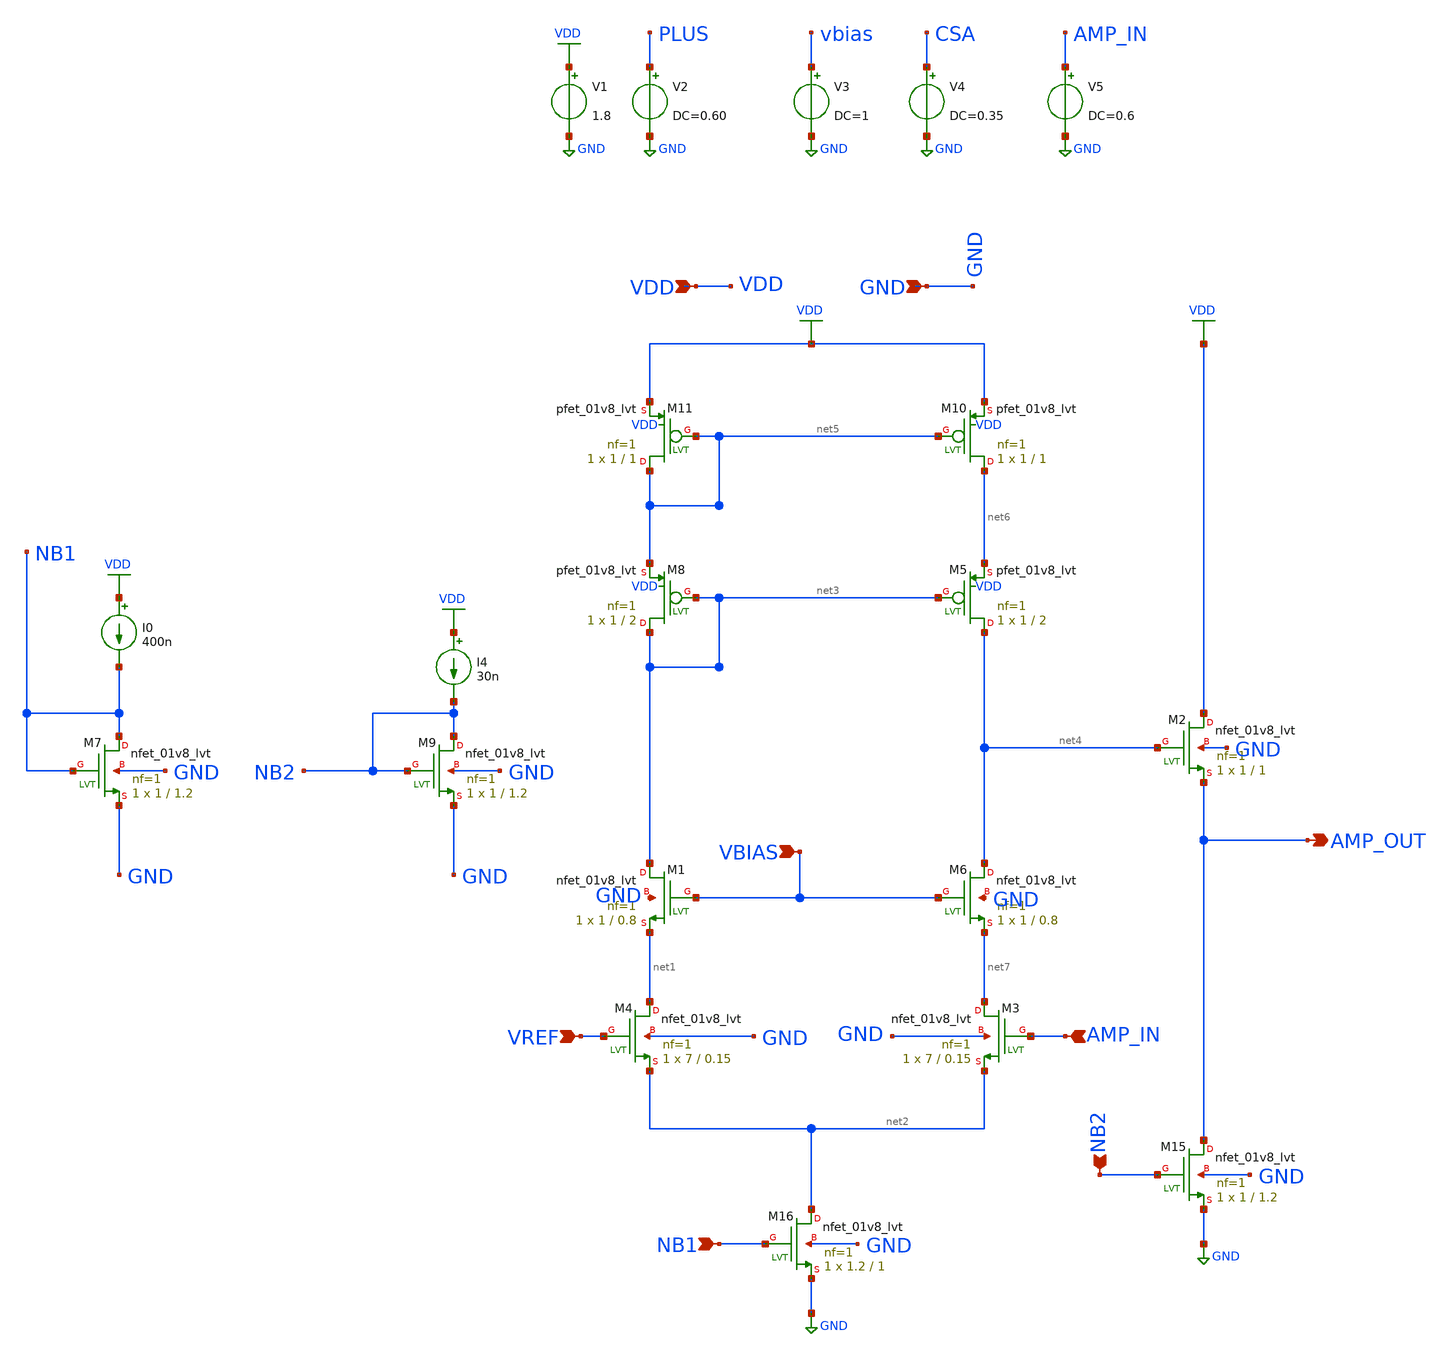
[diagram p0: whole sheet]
** sch_path: xschem/testbench/nmos_cs.sch
**.subckt nmos_cs VREF AMP_IN NB1 VBIAS VDD GND AMP_OUT NB2
*.ipin VREF
*.ipin AMP_IN
*.ipin NB1
*.ipin VBIAS
*.ipin VDD
*.ipin GND
*.opin AMP_OUT
*.ipin NB2
V1 VDD GND 1.8
V2 PLUS GND DC=0.60
V3 vbias GND DC=1
V4 CSA GND DC=0.35
XM8 net3 net3 net5 VDD sky130_fd_pr__pfet_01v8_lvt L=2 W=1 nf=1 ad='int((nf+1)/2) * W/nf * 0.29' as='int((nf+2)/2) * W/nf * 0.29'
+ pd='2*int((nf+1)/2) * (W/nf + 0.29)' ps='2*int((nf+2)/2) * (W/nf + 0.29)' nrd='0.29 / W' nrs='0.29 / W'
+ sa=0 sb=0 sd=0 mult=1 m=1
XM10 net6 net5 VDD VDD sky130_fd_pr__pfet_01v8_lvt L=1 W=1 nf=1 ad='int((nf+1)/2) * W/nf * 0.29' as='int((nf+2)/2) * W/nf * 0.29'
+ pd='2*int((nf+1)/2) * (W/nf + 0.29)' ps='2*int((nf+2)/2) * (W/nf + 0.29)' nrd='0.29 / W' nrs='0.29 / W'
+ sa=0 sb=0 sd=0 mult=1 m=1
XM11 net5 net5 VDD VDD sky130_fd_pr__pfet_01v8_lvt L=1 W=1 nf=1 ad='int((nf+1)/2) * W/nf * 0.29' as='int((nf+2)/2) * W/nf * 0.29'
+ pd='2*int((nf+1)/2) * (W/nf + 0.29)' ps='2*int((nf+2)/2) * (W/nf + 0.29)' nrd='0.29 / W' nrs='0.29 / W'
+ sa=0 sb=0 sd=0 mult=1 m=1
XM16 net2 NB1 GND GND sky130_fd_pr__nfet_01v8_lvt L=1 W=1.2 nf=1 ad='int((nf+1)/2) * W/nf * 0.29' as='int((nf+2)/2) * W/nf * 0.29'
+ pd='2*int((nf+1)/2) * (W/nf + 0.29)' ps='2*int((nf+2)/2) * (W/nf + 0.29)' nrd='0.29 / W' nrs='0.29 / W'
+ sa=0 sb=0 sd=0 mult=1 m=1
XM4 net1 VREF net2 GND sky130_fd_pr__nfet_01v8_lvt L=0.15 W=7 nf=1 ad='int((nf+1)/2) * W/nf * 0.29' as='int((nf+2)/2) * W/nf * 0.29'
+ pd='2*int((nf+1)/2) * (W/nf + 0.29)' ps='2*int((nf+2)/2) * (W/nf + 0.29)' nrd='0.29 / W' nrs='0.29 / W'
+ sa=0 sb=0 sd=0 mult=1 m=1
XM5 net4 net3 net6 VDD sky130_fd_pr__pfet_01v8_lvt L=2 W=1 nf=1 ad='int((nf+1)/2) * W/nf * 0.29' as='int((nf+2)/2) * W/nf * 0.29'
+ pd='2*int((nf+1)/2) * (W/nf + 0.29)' ps='2*int((nf+2)/2) * (W/nf + 0.29)' nrd='0.29 / W' nrs='0.29 / W'
+ sa=0 sb=0 sd=0 mult=1 m=1
XM1 net3 VBIAS net1 GND sky130_fd_pr__nfet_01v8_lvt L=0.8 W=1 nf=1 ad='int((nf+1)/2) * W/nf * 0.29' as='int((nf+2)/2) * W/nf * 0.29'
+ pd='2*int((nf+1)/2) * (W/nf + 0.29)' ps='2*int((nf+2)/2) * (W/nf + 0.29)' nrd='0.29 / W' nrs='0.29 / W'
+ sa=0 sb=0 sd=0 mult=1 m=1
XM3 net7 AMP_IN net2 GND sky130_fd_pr__nfet_01v8_lvt L=0.15 W=7 nf=1 ad='int((nf+1)/2) * W/nf * 0.29'
+ as='int((nf+2)/2) * W/nf * 0.29' pd='2*int((nf+1)/2) * (W/nf + 0.29)' ps='2*int((nf+2)/2) * (W/nf + 0.29)'
+ nrd='0.29 / W' nrs='0.29 / W' sa=0 sb=0 sd=0 mult=1 m=1
XM6 net4 VBIAS net7 GND sky130_fd_pr__nfet_01v8_lvt L=0.8 W=1 nf=1 ad='int((nf+1)/2) * W/nf * 0.29' as='int((nf+2)/2) * W/nf * 0.29'
+ pd='2*int((nf+1)/2) * (W/nf + 0.29)' ps='2*int((nf+2)/2) * (W/nf + 0.29)' nrd='0.29 / W' nrs='0.29 / W'
+ sa=0 sb=0 sd=0 mult=1 m=1
XM2 VDD net4 AMP_OUT GND sky130_fd_pr__nfet_01v8_lvt L=1 W=1 nf=1 ad='int((nf+1)/2) * W/nf * 0.29' as='int((nf+2)/2) * W/nf * 0.29'
+ pd='2*int((nf+1)/2) * (W/nf + 0.29)' ps='2*int((nf+2)/2) * (W/nf + 0.29)' nrd='0.29 / W' nrs='0.29 / W'
+ sa=0 sb=0 sd=0 mult=1 m=1
XM15 AMP_OUT NB2 GND GND sky130_fd_pr__nfet_01v8_lvt L=1.2 W=1 nf=1 ad='int((nf+1)/2) * W/nf * 0.29'
+ as='int((nf+2)/2) * W/nf * 0.29' pd='2*int((nf+1)/2) * (W/nf + 0.29)' ps='2*int((nf+2)/2) * (W/nf + 0.29)'
+ nrd='0.29 / W' nrs='0.29 / W' sa=0 sb=0 sd=0 mult=1 m=1
XM7 NB1 NB1 GND GND sky130_fd_pr__nfet_01v8_lvt L=1.2 W=1 nf=1 ad='int((nf+1)/2) * W/nf * 0.29' as='int((nf+2)/2) * W/nf * 0.29'
+ pd='2*int((nf+1)/2) * (W/nf + 0.29)' ps='2*int((nf+2)/2) * (W/nf + 0.29)' nrd='0.29 / W' nrs='0.29 / W'
+ sa=0 sb=0 sd=0 mult=1 m=1
I0 VDD NB1 400n
I4 VDD NB2 30n
XM9 NB2 NB2 GND GND sky130_fd_pr__nfet_01v8_lvt L=1.2 W=1 nf=1 ad='int((nf+1)/2) * W/nf * 0.29' as='int((nf+2)/2) * W/nf * 0.29'
+ pd='2*int((nf+1)/2) * (W/nf + 0.29)' ps='2*int((nf+2)/2) * (W/nf + 0.29)' nrd='0.29 / W' nrs='0.29 / W'
+ sa=0 sb=0 sd=0 mult=1 m=1
V5 AMP_IN GND DC=0.6
**** begin user architecture code

** opencircuitdesign pdks install
.lib $::SKYWATER_MODELS/sky130.lib.spice tt


**** end user architecture code
**.ends
.GLOBAL GND
.GLOBAL VDD
**** begin user architecture code


.options gmin=0.0000000000000000000001
*.options savecurrents

.control
save all

tran 1m 50m
*plot v(test)
plot v(pix_out)

*noise v(PIX_OUT) V8 dec 10 1 1Meg
*setplot noise2
*print onoise_total

*noise v(PIX_OUT) V8 dec 10 1 1Meg
*setplot noise2
*print onoise_total
.endc


**** end user architecture code
.end
